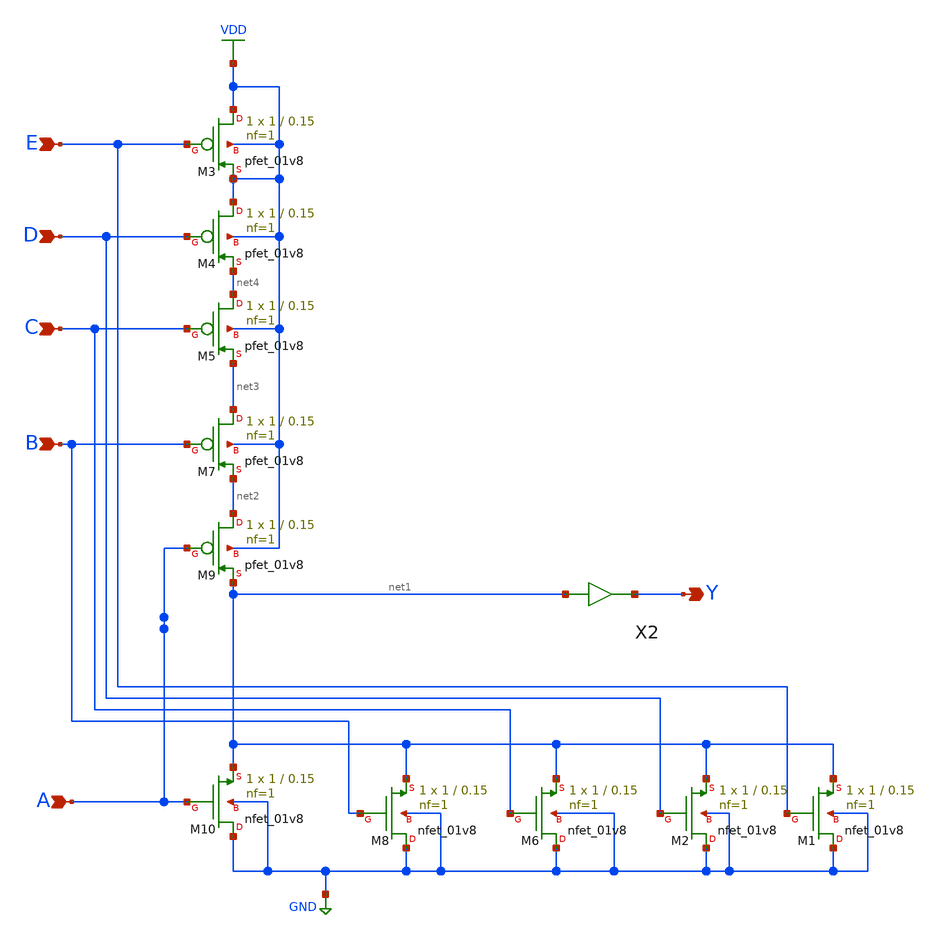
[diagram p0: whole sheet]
** sch_path: gates/OR5.sch
**.subckt OR5 A B Y C D E
*.ipin A
*.ipin B
*.opin Y
*.ipin C
*.ipin D
*.ipin E
XM1 GND E net1 GND sky130_fd_pr__nfet_01v8 L=0.15 W=1 nf=1 ad='int((nf+1)/2) * W/nf * 0.29' as='int((nf+2)/2) * W/nf * 0.29'
+ pd='2*int((nf+1)/2) * (W/nf + 0.29)' ps='2*int((nf+2)/2) * (W/nf + 0.29)' nrd='0.29 / W' nrs='0.29 / W'
+ sa=0 sb=0 sd=0 mult=1 m=1
XM2 GND D net1 GND sky130_fd_pr__nfet_01v8 L=0.15 W=1 nf=1 ad='int((nf+1)/2) * W/nf * 0.29' as='int((nf+2)/2) * W/nf * 0.29'
+ pd='2*int((nf+1)/2) * (W/nf + 0.29)' ps='2*int((nf+2)/2) * (W/nf + 0.29)' nrd='0.29 / W' nrs='0.29 / W'
+ sa=0 sb=0 sd=0 mult=1 m=1
XM3 VDD E VDD VDD sky130_fd_pr__pfet_01v8 L=0.15 W=1 nf=1 ad='int((nf+1)/2) * W/nf * 0.29' as='int((nf+2)/2) * W/nf * 0.29'
+ pd='2*int((nf+1)/2) * (W/nf + 0.29)' ps='2*int((nf+2)/2) * (W/nf + 0.29)' nrd='0.29 / W' nrs='0.29 / W'
+ sa=0 sb=0 sd=0 mult=1 m=1
XM4 VDD D net4 VDD sky130_fd_pr__pfet_01v8 L=0.15 W=1 nf=1 ad='int((nf+1)/2) * W/nf * 0.29' as='int((nf+2)/2) * W/nf * 0.29'
+ pd='2*int((nf+1)/2) * (W/nf + 0.29)' ps='2*int((nf+2)/2) * (W/nf + 0.29)' nrd='0.29 / W' nrs='0.29 / W'
+ sa=0 sb=0 sd=0 mult=1 m=1
XM5 net4 C net3 VDD sky130_fd_pr__pfet_01v8 L=0.15 W=1 nf=1 ad='int((nf+1)/2) * W/nf * 0.29' as='int((nf+2)/2) * W/nf * 0.29'
+ pd='2*int((nf+1)/2) * (W/nf + 0.29)' ps='2*int((nf+2)/2) * (W/nf + 0.29)' nrd='0.29 / W' nrs='0.29 / W'
+ sa=0 sb=0 sd=0 mult=1 m=1
XM6 GND C net1 GND sky130_fd_pr__nfet_01v8 L=0.15 W=1 nf=1 ad='int((nf+1)/2) * W/nf * 0.29' as='int((nf+2)/2) * W/nf * 0.29'
+ pd='2*int((nf+1)/2) * (W/nf + 0.29)' ps='2*int((nf+2)/2) * (W/nf + 0.29)' nrd='0.29 / W' nrs='0.29 / W'
+ sa=0 sb=0 sd=0 mult=1 m=1
XM7 net3 B net2 VDD sky130_fd_pr__pfet_01v8 L=0.15 W=1 nf=1 ad='int((nf+1)/2) * W/nf * 0.29' as='int((nf+2)/2) * W/nf * 0.29'
+ pd='2*int((nf+1)/2) * (W/nf + 0.29)' ps='2*int((nf+2)/2) * (W/nf + 0.29)' nrd='0.29 / W' nrs='0.29 / W'
+ sa=0 sb=0 sd=0 mult=1 m=1
XM8 GND B net1 GND sky130_fd_pr__nfet_01v8 L=0.15 W=1 nf=1 ad='int((nf+1)/2) * W/nf * 0.29' as='int((nf+2)/2) * W/nf * 0.29'
+ pd='2*int((nf+1)/2) * (W/nf + 0.29)' ps='2*int((nf+2)/2) * (W/nf + 0.29)' nrd='0.29 / W' nrs='0.29 / W'
+ sa=0 sb=0 sd=0 mult=1 m=1
XM9 net2 A net1 VDD sky130_fd_pr__pfet_01v8 L=0.15 W=1 nf=1 ad='int((nf+1)/2) * W/nf * 0.29' as='int((nf+2)/2) * W/nf * 0.29'
+ pd='2*int((nf+1)/2) * (W/nf + 0.29)' ps='2*int((nf+2)/2) * (W/nf + 0.29)' nrd='0.29 / W' nrs='0.29 / W'
+ sa=0 sb=0 sd=0 mult=1 m=1
XM10 GND A net1 GND sky130_fd_pr__nfet_01v8 L=0.15 W=1 nf=1 ad='int((nf+1)/2) * W/nf * 0.29' as='int((nf+2)/2) * W/nf * 0.29'
+ pd='2*int((nf+1)/2) * (W/nf + 0.29)' ps='2*int((nf+2)/2) * (W/nf + 0.29)' nrd='0.29 / W' nrs='0.29 / W'
+ sa=0 sb=0 sd=0 mult=1 m=1
X2 net1 Y inv_vtc
**.ends

* expanding   symbol:  /home/apn/test_xschem_sky130/inv_vtc.sym # of pins=2
** sym_path: gates/inv_vtc.sym
** sch_path: gates/inv_vtc.sch
.subckt inv_vtc A Y
*.ipin A
*.opin Y
XM1 Y A VDD VDD sky130_fd_pr__pfet_01v8 L=0.15 W=2 nf=1 ad='int((nf+1)/2) * W/nf * 0.29' as='int((nf+2)/2) * W/nf * 0.29'
+ pd='2*int((nf+1)/2) * (W/nf + 0.29)' ps='2*int((nf+2)/2) * (W/nf + 0.29)' nrd='0.29 / W' nrs='0.29 / W'
+ sa=0 sb=0 sd=0 mult=1 m=1
XM2 Y A GND GND sky130_fd_pr__nfet_01v8 L=0.15 W=1 nf=1 ad='int((nf+1)/2) * W/nf * 0.29' as='int((nf+2)/2) * W/nf * 0.29'
+ pd='2*int((nf+1)/2) * (W/nf + 0.29)' ps='2*int((nf+2)/2) * (W/nf + 0.29)' nrd='0.29 / W' nrs='0.29 / W'
+ sa=0 sb=0 sd=0 mult=1 m=1
.ends

.GLOBAL VDD
.GLOBAL GND
.end
